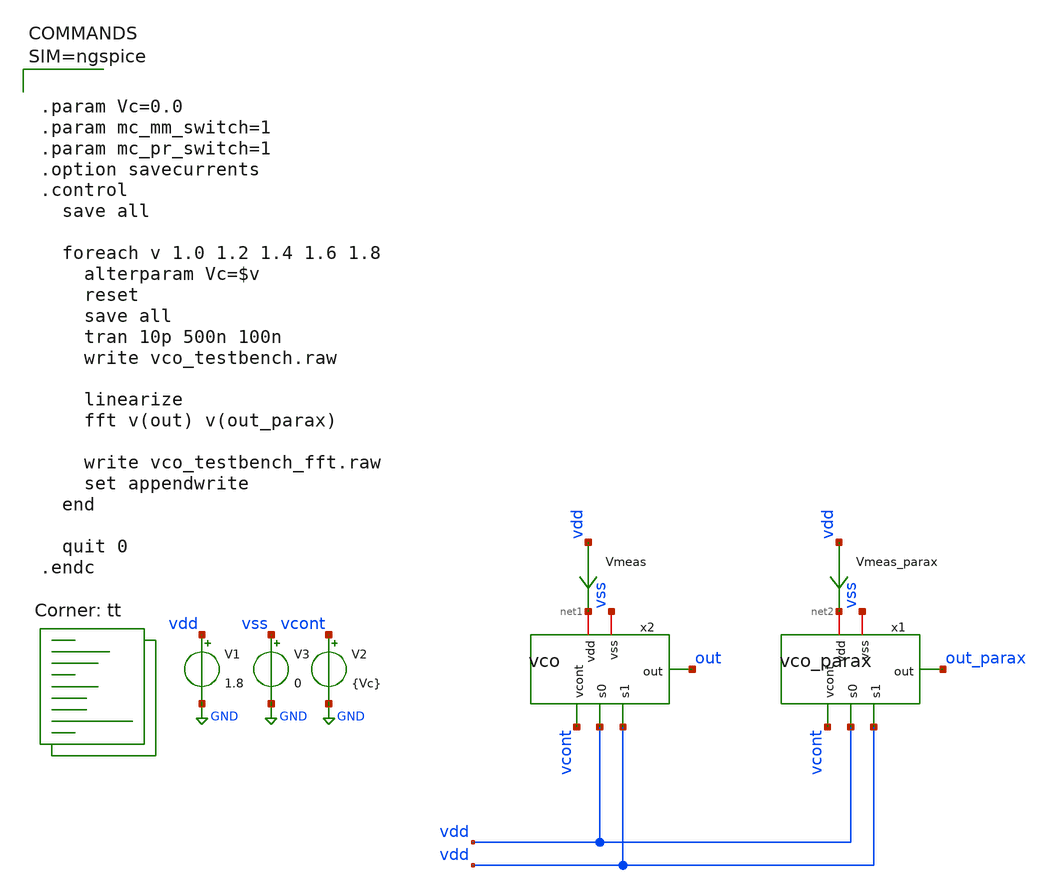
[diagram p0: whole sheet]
** sch_path: xschem/vco_testbench.sch
**.subckt vco_testbench
V1 vdd GND 1.8
V2 vcont GND {Vc}
x2 net1 vcont vdd vdd out vss vco
V3 vss GND 0
x1 net2 vcont vdd vdd out_parax vss vco_parax
Vmeas vdd net1 0
.save i(vmeas)
Vmeas_parax vdd net2 0
.save i(vmeas_parax)
**** begin user architecture code
.lib $::SKYWATER_MODELS/sky130.lib.spice tt



.param Vc=0.0
.param mc_mm_switch=1
.param mc_pr_switch=1
.option savecurrents
.control
  save all

  foreach v 1.0 1.2 1.4 1.6 1.8
    alterparam Vc=$v
    reset
    save all
    tran 10p 500n 100n
    write vco_testbench.raw

    linearize
    fft v(out) v(out_parax)

    write vco_testbench_fft.raw
    set appendwrite
  end

  quit 0
.endc



**** end user architecture code
**.ends

* expanding   symbol:  vco.sym # of pins=6
** sym_path: xschem/vco.sym
** sch_path: xschem/vco.sch
.subckt vco vdd vcont s0 s1 out vss
*.opin out
*.iopin vdd
*.ipin s0
*.ipin s1
*.ipin vcont
*.iopin vss
x1 vdd vcont_b s0 s1 stage_0_out net1 vcont vss delay_stage
x2 vdd vcont_b s0 s1 stage_1_out stage_0_out vcont vss delay_stage
x3 vdd vcont_b s0 s1 net1 stage_1_out vcont vss delay_stage
C1 stage_0_out 0 10f m=1
C2 stage_1_out 0 10f m=1
C3 net1 0 10f m=1
XM5 vcont_b vcont_b vdd vdd sky130_fd_pr__pfet_01v8 L=0.15 W=2 nf=1 ad='int((nf+1)/2) * W/nf * 0.29'
+ as='int((nf+2)/2) * W/nf * 0.29' pd='2*int((nf+1)/2) * (W/nf + 0.29)' ps='2*int((nf+2)/2) * (W/nf + 0.29)'
+ nrd='0.29 / W' nrs='0.29 / W' sa=0 sb=0 sd=0 mult=1 m=1
XM6 vcont_b vcont vss vss sky130_fd_pr__nfet_01v8 L=0.15 W=1 nf=1 ad='int((nf+1)/2) * W/nf * 0.29' as='int((nf+2)/2) * W/nf * 0.29'
+ pd='2*int((nf+1)/2) * (W/nf + 0.29)' ps='2*int((nf+2)/2) * (W/nf + 0.29)' nrd='0.29 / W' nrs='0.29 / W'
+ sa=0 sb=0 sd=0 mult=1 m=1
XM1 out net1 vss vss sky130_fd_pr__nfet_01v8 L=0.15 W=1 nf=1 ad='int((1 + 1)/2) * 1 / 1 * 0.29' as='int((1 + 2)/2) * 1 / 1 * 0.29'
+ pd='2*int((1 + 1)/2) * (1 / 1 + 0.29)' ps='2*int((1 + 2)/2) * (1 / 1 + 0.29)' nrd='0.29 / 1 ' nrs='0.29 / 1 '
+ sa=0 sb=0 sd=0 mult=1 m=1
XM2 out net1 vdd vdd sky130_fd_pr__pfet_01v8 L=0.15 W=2 nf=1 ad='int((nf+1)/2) * W/nf * 0.29' as='int((nf+2)/2) * W/nf * 0.29'
+ pd='2*int((nf+1)/2) * (W/nf + 0.29)' ps='2*int((nf+2)/2) * (W/nf + 0.29)' nrd='0.29 / W' nrs='0.29 / W'
+ sa=0 sb=0 sd=0 mult=1 m=1
.ends


* expanding   symbol:  vco_parax.sym # of pins=6
** sym_path: xschem/vco.sym
.include [file normalize ../mag/vco.sim.spice]

* expanding   symbol:  delay_stage.sym # of pins=8
** sym_path: xschem/delay_stage.sym
** sch_path: xschem/delay_stage.sch
.subckt delay_stage vdd vcont_p s0 s1 out in vcont_n vss
*.ipin in
*.opin out
*.iopin vdd
*.ipin vcont_n
*.ipin vcont_p
*.ipin s0
*.ipin s1
*.iopin vss
XM3 out in net2 vss sky130_fd_pr__nfet_01v8 L=0.15 W=1 nf=1 ad='int((nf+1)/2) * W/nf * 0.29' as='int((nf+2)/2) * W/nf * 0.29'
+ pd='2*int((nf+1)/2) * (W/nf + 0.29)' ps='2*int((nf+2)/2) * (W/nf + 0.29)' nrd='0.29 / W' nrs='0.29 / W'
+ sa=0 sb=0 sd=0 mult=1 m=1
XM2 out in net1 vdd sky130_fd_pr__pfet_01v8 L=0.15 W=2 nf=1 ad='int((nf+1)/2) * W/nf * 0.29' as='int((nf+2)/2) * W/nf * 0.29'
+ pd='2*int((nf+1)/2) * (W/nf + 0.29)' ps='2*int((nf+2)/2) * (W/nf + 0.29)' nrd='0.29 / W' nrs='0.29 / W'
+ sa=0 sb=0 sd=0 mult=1 m=1
XM1 net1 vcont_p vdd vdd sky130_fd_pr__pfet_01v8 L=0.15 W=2 nf=1 ad='int((nf+1)/2) * W/nf * 0.29' as='int((nf+2)/2) * W/nf * 0.29'
+ pd='2*int((nf+1)/2) * (W/nf + 0.29)' ps='2*int((nf+2)/2) * (W/nf + 0.29)' nrd='0.29 / W' nrs='0.29 / W'
+ sa=0 sb=0 sd=0 mult=1 m=1
XM4 net2 vcont_n vss vss sky130_fd_pr__nfet_01v8 L=0.15 W=1 nf=1 ad='int((nf+1)/2) * W/nf * 0.29' as='int((nf+2)/2) * W/nf * 0.29'
+ pd='2*int((nf+1)/2) * (W/nf + 0.29)' ps='2*int((nf+2)/2) * (W/nf + 0.29)' nrd='0.29 / W' nrs='0.29 / W'
+ sa=0 sb=0 sd=0 mult=1 m=1
XC2 net3 vss sky130_fd_pr__cap_mim_m3_1 W=2.1 L=2.1 MF=1 m=1
XC1 net4 vss sky130_fd_pr__cap_mim_m3_1 W=2.1 L=4.2 MF=1 m=1
XM5 out s0 net4 vss sky130_fd_pr__nfet_01v8 L=0.15 W=1 nf=1 ad='int((nf+1)/2) * W/nf * 0.29' as='int((nf+2)/2) * W/nf * 0.29'
+ pd='2*int((nf+1)/2) * (W/nf + 0.29)' ps='2*int((nf+2)/2) * (W/nf + 0.29)' nrd='0.29 / W' nrs='0.29 / W'
+ sa=0 sb=0 sd=0 mult=1 m=1
XM6 out s1 net3 vss sky130_fd_pr__nfet_01v8 L=0.15 W=1 nf=1 ad='int((nf+1)/2) * W/nf * 0.29' as='int((nf+2)/2) * W/nf * 0.29'
+ pd='2*int((nf+1)/2) * (W/nf + 0.29)' ps='2*int((nf+2)/2) * (W/nf + 0.29)' nrd='0.29 / W' nrs='0.29 / W'
+ sa=0 sb=0 sd=0 mult=1 m=1
.ends

.GLOBAL GND
.end
